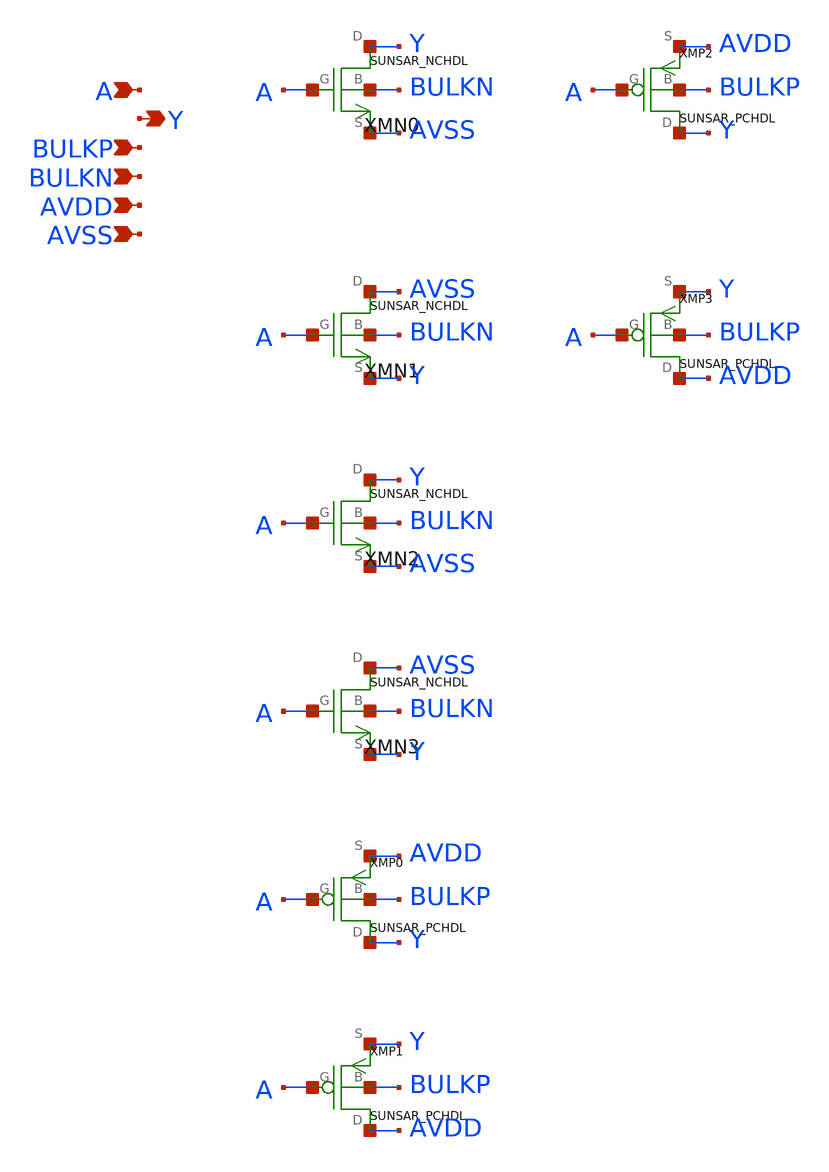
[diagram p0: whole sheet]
** sch_path: ip/sun_sar9b_sky130nm/design/SUN_SAR9B_SKY130NM/SUNSAR_IVX4_CV.sch
**.subckt SUNSAR_IVX4_CV A Y BULKP BULKN AVDD AVSS
*.ipin A
*.opin Y
*.ipin BULKP
*.ipin BULKN
*.ipin AVDD
*.ipin AVSS
XMN0 Y A AVSS BULKN SUNSAR_NCHDL
XMN1 AVSS A Y BULKN SUNSAR_NCHDL
XMN2 Y A AVSS BULKN SUNSAR_NCHDL
XMN3 AVSS A Y BULKN SUNSAR_NCHDL
XMP0 Y A AVDD BULKP SUNSAR_PCHDL
XMP1 AVDD A Y BULKP SUNSAR_PCHDL
XMP2 Y A AVDD BULKP SUNSAR_PCHDL
XMP3 AVDD A Y BULKP SUNSAR_PCHDL
**.ends
.end
